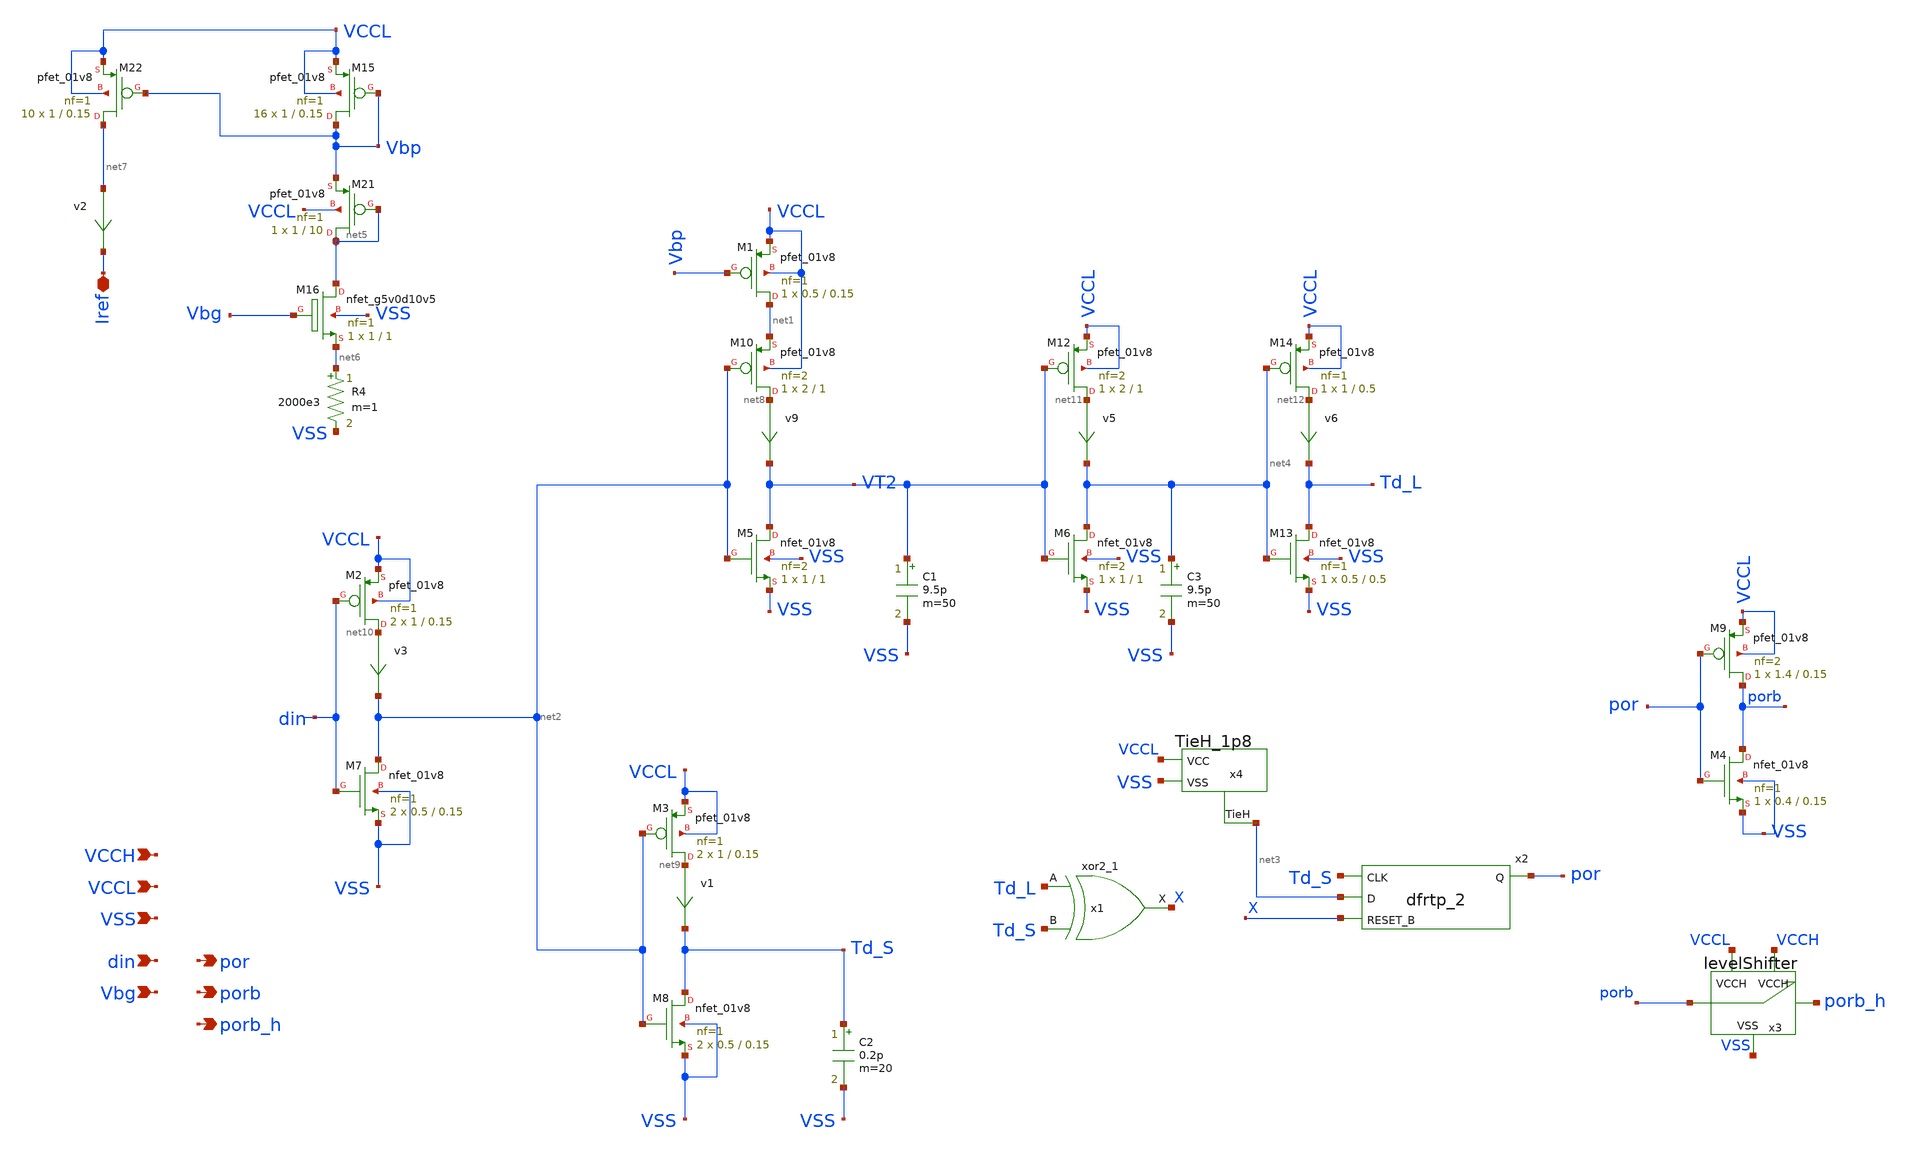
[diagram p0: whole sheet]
** sch_path: xschem/delayPulse.sch
**.subckt delayPulse VCCL VSS din Vbg por VCCH porb porb_h Iref
*.ipin VCCL
*.ipin VSS
*.ipin din
*.ipin Vbg
*.opin por
*.ipin VCCH
*.opin porb
*.opin porb_h
*.iopin Iref
v9 net8 VT2 0
.save i(v9)
v1 net9 Td_S 0
.save i(v1)
C1 VT2 VSS 9.5p m=50
x2 Td_S net3 X VSS VSS VCCL VCCL por sky130_fd_sc_hd__dfrtp_2
v3 net10 net2 0
.save i(v3)
C2 Td_S VSS 0.2p m=20
x1 Td_L Td_S VSS VSS VCCL VCCL X sky130_fd_sc_hd__xor2_1
x3 porb porb_h VCCL VSS VCCH levelShifter
XM1 net1 Vbp VCCL VCCL sky130_fd_pr__pfet_01v8 L=0.15 W=0.5 nf=1 ad='int((nf+1)/2) * W/nf * 0.29' as='int((nf+2)/2) * W/nf * 0.29'
+ pd='2*int((nf+1)/2) * (W/nf + 0.29)' ps='2*int((nf+2)/2) * (W/nf + 0.29)' nrd='0.29 / W' nrs='0.29 / W'
+ sa=0 sb=0 sd=0 mult=1 m=1
XM2 net10 din VCCL VCCL sky130_fd_pr__pfet_01v8 L=0.15 W=1 nf=1 ad='int((nf+1)/2) * W/nf * 0.29' as='int((nf+2)/2) * W/nf * 0.29'
+ pd='2*int((nf+1)/2) * (W/nf + 0.29)' ps='2*int((nf+2)/2) * (W/nf + 0.29)' nrd='0.29 / W' nrs='0.29 / W'
+ sa=0 sb=0 sd=0 mult=2 m=2
XM3 net9 net2 VCCL VCCL sky130_fd_pr__pfet_01v8 L=0.15 W=1 nf=1 ad='int((nf+1)/2) * W/nf * 0.29' as='int((nf+2)/2) * W/nf * 0.29'
+ pd='2*int((nf+1)/2) * (W/nf + 0.29)' ps='2*int((nf+2)/2) * (W/nf + 0.29)' nrd='0.29 / W' nrs='0.29 / W'
+ sa=0 sb=0 sd=0 mult=2 m=2
XM5 VT2 net2 VSS VSS sky130_fd_pr__nfet_01v8 L=1 W=1 nf=2 ad='int((nf+1)/2) * W/nf * 0.29' as='int((nf+2)/2) * W/nf * 0.29'
+ pd='2*int((nf+1)/2) * (W/nf + 0.29)' ps='2*int((nf+2)/2) * (W/nf + 0.29)' nrd='0.29 / W' nrs='0.29 / W'
+ sa=0 sb=0 sd=0 mult=1 m=1
XM7 net2 din VSS VSS sky130_fd_pr__nfet_01v8 L=0.15 W=0.5 nf=1 ad='int((nf+1)/2) * W/nf * 0.29' as='int((nf+2)/2) * W/nf * 0.29'
+ pd='2*int((nf+1)/2) * (W/nf + 0.29)' ps='2*int((nf+2)/2) * (W/nf + 0.29)' nrd='0.29 / W' nrs='0.29 / W'
+ sa=0 sb=0 sd=0 mult=2 m=2
XM8 Td_S net2 VSS VSS sky130_fd_pr__nfet_01v8 L=0.15 W=0.5 nf=1 ad='int((nf+1)/2) * W/nf * 0.29' as='int((nf+2)/2) * W/nf * 0.29'
+ pd='2*int((nf+1)/2) * (W/nf + 0.29)' ps='2*int((nf+2)/2) * (W/nf + 0.29)' nrd='0.29 / W' nrs='0.29 / W'
+ sa=0 sb=0 sd=0 mult=2 m=2
XM10 net8 net2 net1 VCCL sky130_fd_pr__pfet_01v8 L=1 W=2 nf=2 ad='int((nf+1)/2) * W/nf * 0.29' as='int((nf+2)/2) * W/nf * 0.29'
+ pd='2*int((nf+1)/2) * (W/nf + 0.29)' ps='2*int((nf+2)/2) * (W/nf + 0.29)' nrd='0.29 / W' nrs='0.29 / W'
+ sa=0 sb=0 sd=0 mult=1 m=1
v5 net11 net4 0
.save i(v5)
XM6 net4 VT2 VSS VSS sky130_fd_pr__nfet_01v8 L=1 W=1 nf=2 ad='int((nf+1)/2) * W/nf * 0.29' as='int((nf+2)/2) * W/nf * 0.29'
+ pd='2*int((nf+1)/2) * (W/nf + 0.29)' ps='2*int((nf+2)/2) * (W/nf + 0.29)' nrd='0.29 / W' nrs='0.29 / W'
+ sa=0 sb=0 sd=0 mult=1 m=1
XM12 net11 VT2 VCCL VCCL sky130_fd_pr__pfet_01v8 L=1 W=2 nf=2 ad='int((nf+1)/2) * W/nf * 0.29' as='int((nf+2)/2) * W/nf * 0.29'
+ pd='2*int((nf+1)/2) * (W/nf + 0.29)' ps='2*int((nf+2)/2) * (W/nf + 0.29)' nrd='0.29 / W' nrs='0.29 / W'
+ sa=0 sb=0 sd=0 mult=1 m=1
v6 net12 Td_L 0
.save i(v6)
XM13 Td_L net4 VSS VSS sky130_fd_pr__nfet_01v8 L=0.5 W=0.5 nf=1 ad='int((nf+1)/2) * W/nf * 0.29' as='int((nf+2)/2) * W/nf * 0.29'
+ pd='2*int((nf+1)/2) * (W/nf + 0.29)' ps='2*int((nf+2)/2) * (W/nf + 0.29)' nrd='0.29 / W' nrs='0.29 / W'
+ sa=0 sb=0 sd=0 mult=1 m=1
XM14 net12 net4 VCCL VCCL sky130_fd_pr__pfet_01v8 L=0.5 W=1 nf=1 ad='int((nf+1)/2) * W/nf * 0.29' as='int((nf+2)/2) * W/nf * 0.29'
+ pd='2*int((nf+1)/2) * (W/nf + 0.29)' ps='2*int((nf+2)/2) * (W/nf + 0.29)' nrd='0.29 / W' nrs='0.29 / W'
+ sa=0 sb=0 sd=0 mult=1 m=1
C3 net4 VSS 9.5p m=50
x4 net3 VSS VCCL TieH_1p8
XM4 porb por VSS VSS sky130_fd_pr__nfet_01v8 L=0.15 W=0.4 nf=1 ad='int((nf+1)/2) * W/nf * 0.29' as='int((nf+2)/2) * W/nf * 0.29'
+ pd='2*int((nf+1)/2) * (W/nf + 0.29)' ps='2*int((nf+2)/2) * (W/nf + 0.29)' nrd='0.29 / W' nrs='0.29 / W'
+ sa=0 sb=0 sd=0 mult=1 m=1
XM9 porb por VCCL VCCL sky130_fd_pr__pfet_01v8 L=0.15 W=1.4 nf=2 ad='int((nf+1)/2) * W/nf * 0.29' as='int((nf+2)/2) * W/nf * 0.29'
+ pd='2*int((nf+1)/2) * (W/nf + 0.29)' ps='2*int((nf+2)/2) * (W/nf + 0.29)' nrd='0.29 / W' nrs='0.29 / W'
+ sa=0 sb=0 sd=0 mult=1 m=1
XM15 Vbp Vbp VCCL VCCL sky130_fd_pr__pfet_01v8 L=0.15 W=1 nf=1 ad='int((nf+1)/2) * W/nf * 0.29' as='int((nf+2)/2) * W/nf * 0.29'
+ pd='2*int((nf+1)/2) * (W/nf + 0.29)' ps='2*int((nf+2)/2) * (W/nf + 0.29)' nrd='0.29 / W' nrs='0.29 / W'
+ sa=0 sb=0 sd=0 mult=16 m=16
XM16 net5 Vbg net6 VSS sky130_fd_pr__nfet_g5v0d10v5 L=1 W=1 nf=1 ad='int((nf+1)/2) * W/nf * 0.29' as='int((nf+2)/2) * W/nf * 0.29'
+ pd='2*int((nf+1)/2) * (W/nf + 0.29)' ps='2*int((nf+2)/2) * (W/nf + 0.29)' nrd='0.29 / W' nrs='0.29 / W'
+ sa=0 sb=0 sd=0 mult=1 m=1
XM21 net5 net5 Vbp VCCL sky130_fd_pr__pfet_01v8 L=10 W=1 nf=1 ad='int((nf+1)/2) * W/nf * 0.29' as='int((nf+2)/2) * W/nf * 0.29'
+ pd='2*int((nf+1)/2) * (W/nf + 0.29)' ps='2*int((nf+2)/2) * (W/nf + 0.29)' nrd='0.29 / W' nrs='0.29 / W'
+ sa=0 sb=0 sd=0 mult=1 m=1
R4 net6 VSS 2000e3 m=1
XM22 net7 Vbp VCCL VCCL sky130_fd_pr__pfet_01v8 L=0.15 W=1 nf=1 ad='int((nf+1)/2) * W/nf * 0.29' as='int((nf+2)/2) * W/nf * 0.29'
+ pd='2*int((nf+1)/2) * (W/nf + 0.29)' ps='2*int((nf+2)/2) * (W/nf + 0.29)' nrd='0.29 / W' nrs='0.29 / W'
+ sa=0 sb=0 sd=0 mult=10 m=10
v2 net7 Iref 0
.save i(v2)
**.ends
.end
